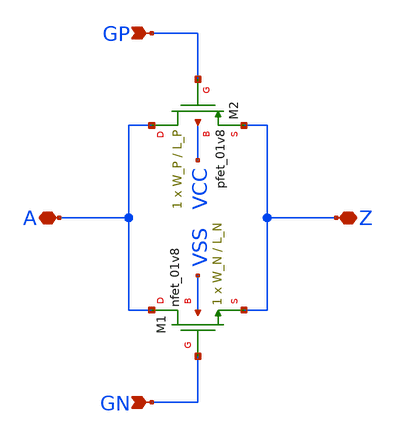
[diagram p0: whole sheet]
** sch_path: sky130_tests/passgate.sch
**.subckt passgate A Z GP GN
*.iopin A
*.iopin Z
*.ipin GP
*.ipin GN
XM1 A GN Z VSS sky130_fd_pr__nfet_01v8 W=W_N L=L_N ad='W * 0.29' pd='W + 2 * 0.29' as='W * 0.29' ps='W + 2 * 0.29'
+ nrd=0 nrs=0 sa=0 sb=0 sd=0 nf=1 mult=1
XM2 A GP Z VCC sky130_fd_pr__pfet_01v8 W=W_P L=L_P ad='W * 0.29' pd='W + 2 * 0.29' as='W * 0.29' ps='W + 2 * 0.29'
+ nrd=0 nrs=0 sa=0 sb=0 sd=0 nf=1 mult=1
**.ends
.end
